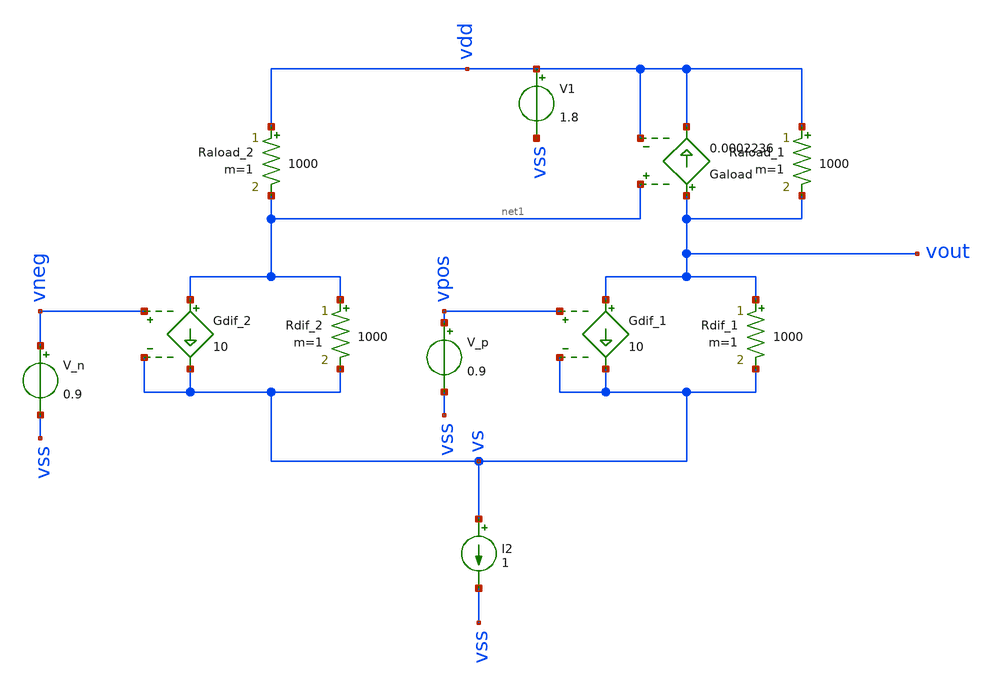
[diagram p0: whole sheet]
** sch_path: test-python/result_comp/xschem/ota.sch
**.subckt ota
Rdif_2 net1 vs 1000 m=1
Gdif_2 net1 vs vneg vs 10
Rdif_1 vout vs 1000 m=1
Gdif_1 vout vs vpos vs 10
I2 vs vss 1
V1 vdd vss 1.8
V_n vneg vss 0.9
V_p vpos vss 0.9
Raload_1 vdd vout 1000 m=1
Raload_2 vdd net1 1000 m=1
Gaload vout vdd net1 vdd 0.0002236
**.ends
.end
